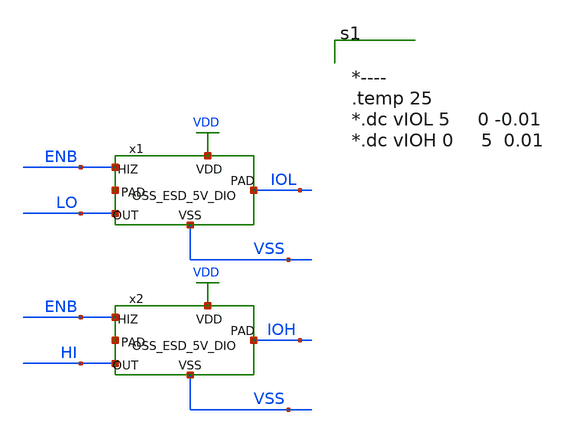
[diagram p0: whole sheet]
** sch_path: schematic/TB/IO_DC.sch
**.subckt IO_DC
x1 VDD IOL VSS ENB LO OSS_ESD_5V_DIO
x2 VDD IOH VSS ENB HI OSS_ESD_5V_DIO
**** begin user architecture code



* ngspice commands
.include '~/Dropbox/91_OpenPDK/TR-1um/libs.tech/spice/models/ip62_models'
.param vdd=5.0
.param vss=0
*----
vdd  vdd 0 dc vdd
vss  vss 0 dc vss
venb enb 0 dc vdd
*----
vHI  HI  0 dc vdd
vLO  LO  0 dc vss
*----
vIOH IOH  0 dc vdd
vIOL IOL  0 dc vdd



**** end user architecture code
**.ends
.GLOBAL VDD
**** begin user architecture code


*----
.temp 25
*.dc vIOL 5     0 -0.01
*.dc vIOH 0     5  0.01


**** end user architecture code
.end
